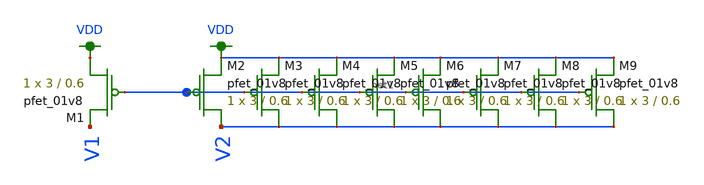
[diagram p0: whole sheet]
** sch_path: schematic/bandgap_current_mirror_lvs.sch
**.subckt bandgap_current_mirror_lvs
XM1 VDD net1 V1 VDD sky130_fd_pr__pfet_01v8 L=0.6 W=3 nf=1 ad='int((nf+1)/2) * W/nf * 0.29' as='int((nf+2)/2) * W/nf * 0.29'
+ pd='2*int((nf+1)/2) * (W/nf + 0.29)' ps='2*int((nf+2)/2) * (W/nf + 0.29)' nrd='0.29 / W' nrs='0.29 / W'
+ sa=0 sb=0 sd=0 mult=1 m=1
XM2 V2 net1 VDD VDD sky130_fd_pr__pfet_01v8 L=0.6 W=3 nf=1 ad='int((nf+1)/2) * W/nf * 0.29' as='int((nf+2)/2) * W/nf * 0.29'
+ pd='2*int((nf+1)/2) * (W/nf + 0.29)' ps='2*int((nf+2)/2) * (W/nf + 0.29)' nrd='0.29 / W' nrs='0.29 / W'
+ sa=0 sb=0 sd=0 mult=1 m=1
XM3 V2 net1 VDD VDD sky130_fd_pr__pfet_01v8 L=0.6 W=3 nf=1 ad='int((nf+1)/2) * W/nf * 0.29' as='int((nf+2)/2) * W/nf * 0.29'
+ pd='2*int((nf+1)/2) * (W/nf + 0.29)' ps='2*int((nf+2)/2) * (W/nf + 0.29)' nrd='0.29 / W' nrs='0.29 / W'
+ sa=0 sb=0 sd=0 mult=1 m=1
XM4 V2 net1 VDD VDD sky130_fd_pr__pfet_01v8 L=0.6 W=3 nf=1 ad='int((nf+1)/2) * W/nf * 0.29' as='int((nf+2)/2) * W/nf * 0.29'
+ pd='2*int((nf+1)/2) * (W/nf + 0.29)' ps='2*int((nf+2)/2) * (W/nf + 0.29)' nrd='0.29 / W' nrs='0.29 / W'
+ sa=0 sb=0 sd=0 mult=1 m=1
XM5 V2 net1 VDD VDD sky130_fd_pr__pfet_01v8 L=0.6 W=3 nf=1 ad='int((nf+1)/2) * W/nf * 0.29' as='int((nf+2)/2) * W/nf * 0.29'
+ pd='2*int((nf+1)/2) * (W/nf + 0.29)' ps='2*int((nf+2)/2) * (W/nf + 0.29)' nrd='0.29 / W' nrs='0.29 / W'
+ sa=0 sb=0 sd=0 mult=1 m=1
XM6 V2 net1 VDD VDD sky130_fd_pr__pfet_01v8 L=0.6 W=3 nf=1 ad='int((nf+1)/2) * W/nf * 0.29' as='int((nf+2)/2) * W/nf * 0.29'
+ pd='2*int((nf+1)/2) * (W/nf + 0.29)' ps='2*int((nf+2)/2) * (W/nf + 0.29)' nrd='0.29 / W' nrs='0.29 / W'
+ sa=0 sb=0 sd=0 mult=1 m=1
XM7 V2 net1 VDD VDD sky130_fd_pr__pfet_01v8 L=0.6 W=3 nf=1 ad='int((nf+1)/2) * W/nf * 0.29' as='int((nf+2)/2) * W/nf * 0.29'
+ pd='2*int((nf+1)/2) * (W/nf + 0.29)' ps='2*int((nf+2)/2) * (W/nf + 0.29)' nrd='0.29 / W' nrs='0.29 / W'
+ sa=0 sb=0 sd=0 mult=1 m=1
XM8 V2 net1 VDD VDD sky130_fd_pr__pfet_01v8 L=0.6 W=3 nf=1 ad='int((nf+1)/2) * W/nf * 0.29' as='int((nf+2)/2) * W/nf * 0.29'
+ pd='2*int((nf+1)/2) * (W/nf + 0.29)' ps='2*int((nf+2)/2) * (W/nf + 0.29)' nrd='0.29 / W' nrs='0.29 / W'
+ sa=0 sb=0 sd=0 mult=1 m=1
XM9 V2 net1 VDD VDD sky130_fd_pr__pfet_01v8 L=0.6 W=3 nf=1 ad='int((nf+1)/2) * W/nf * 0.29' as='int((nf+2)/2) * W/nf * 0.29'
+ pd='2*int((nf+1)/2) * (W/nf + 0.29)' ps='2*int((nf+2)/2) * (W/nf + 0.29)' nrd='0.29 / W' nrs='0.29 / W'
+ sa=0 sb=0 sd=0 mult=1 m=1
**.ends
.GLOBAL VDD
.end
